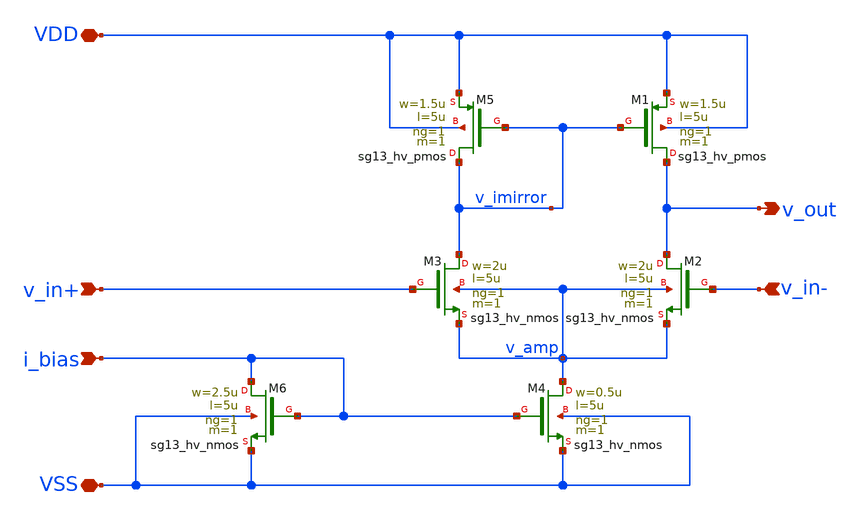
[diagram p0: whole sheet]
** sch_path: 3_Real_Cir/self_build_opamp.sch
**.subckt self_build_opamp v_in+ v_in- v_out VDD VSS i_bias
*.ipin v_in+
*.ipin v_in-
*.opin v_out
*.iopin VDD
*.iopin VSS
*.ipin i_bias
XM3 v_imirror v_in+ v_amp v_amp sg13_hv_nmos w=2u l=5u ng=1 m=1 mm_ok=1
XM2 v_out v_in- v_amp v_amp sg13_hv_nmos w=2u l=5u ng=1 m=1 mm_ok=1
XM4 v_amp i_bias VSS VSS sg13_hv_nmos w=0.5u l=5u ng=1 m=1 mm_ok=1
XM5 v_imirror v_imirror VDD VDD sg13_hv_pmos w=1.5u l=5u ng=1 m=1 mm_ok=1
XM1 v_out v_imirror VDD VDD sg13_hv_pmos w=1.5u l=5u ng=1 m=1 mm_ok=1
XM6 i_bias i_bias VSS VSS sg13_hv_nmos w=2.5u l=5u ng=1 m=1 mm_ok=1
**.ends
.end
